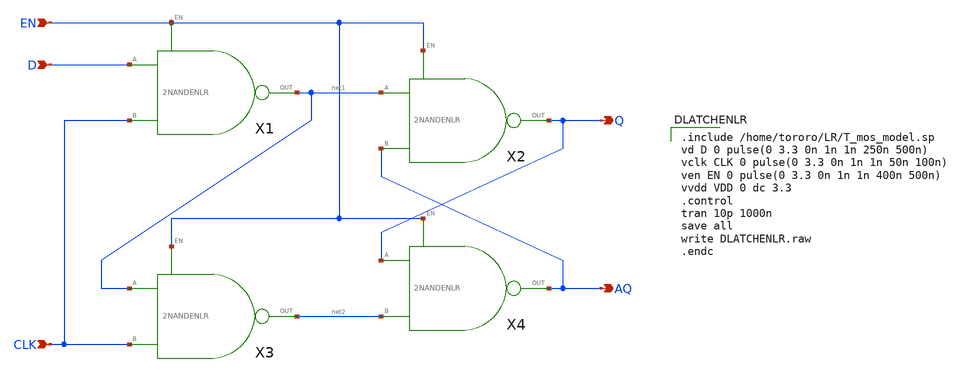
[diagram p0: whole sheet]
** sch_path: task_LATCH/DLATCHENLR.sch
**.subckt DLATCHENLR D CLK Q AQ EN
*.ipin D
*.ipin CLK
*.opin Q
*.opin AQ
*.ipin EN
X1 D CLK net1 EN 2NANDENLR
X2 net1 AQ Q EN 2NANDENLR
X3 net1 CLK net2 EN 2NANDENLR
X4 Q net2 AQ EN 2NANDENLR
**** begin user architecture code

.include /home/tororo/LR/T_mos_model.sp
vd D 0 pulse(0 3.3 0n 1n 1n 250n 500n)
vclk CLK 0 pulse(0 3.3 0n 1n 1n 50n 100n)
ven EN 0 pulse(0 3.3 0n 1n 1n 400n 500n)
vvdd VDD 0 dc 3.3
.control
tran 10p 1000n
save all
write DLATCHENLR.raw
.endc

**** end user architecture code
**.ends

* expanding   symbol:  LR/2NANDENLR.sym # of pins=4
** sym_path: task_LATCH/2NANDENLR.sym
** sch_path: task_LATCH/2NANDENLR.sch
.subckt 2NANDENLR A B OUT EN
*.ipin A
*.ipin B
*.opin OUT
*.ipin EN
M1 OUT A net1 GND nch w=3.5u l=0.35u as=0 ps=0 ad=0 pd=0 m=1
M2 OUT B VDDL VDDL pch w=3.5u l=0.35u as=0 ps=0 ad=0 pd=0 m=1
M3 OUT A VDDL VDDL pch w=3.5u l=0.35u as=0 ps=0 ad=0 pd=0 m=1
M4 net1 B GND GND nch w=3.5u l=0.35u as=0 ps=0 ad=0 pd=0 m=1
M5 VDDL EN VDD VDD pch w=3.5u l=0.35u as=0 ps=0 ad=0 pd=0 m=1
**** begin user architecture code

.include /home/tororo/LR/T_mos_model.sp
va A 0 pulse(0 3.3 0n 1n 1n 250n 500n)
vb B 0 pulse(0 3.3 0n 1n 1n 50n 100n)
ven EN 0 pulse(0 3.3 300n 1n 1n 100n 500n)
vvdd VDD 0 dc 3.3
.control
tran 10p 1000n
save all
write 2NANDENLR.raw
.endc

**** end user architecture code
.ends

.GLOBAL VDD
.GLOBAL GND
.end
